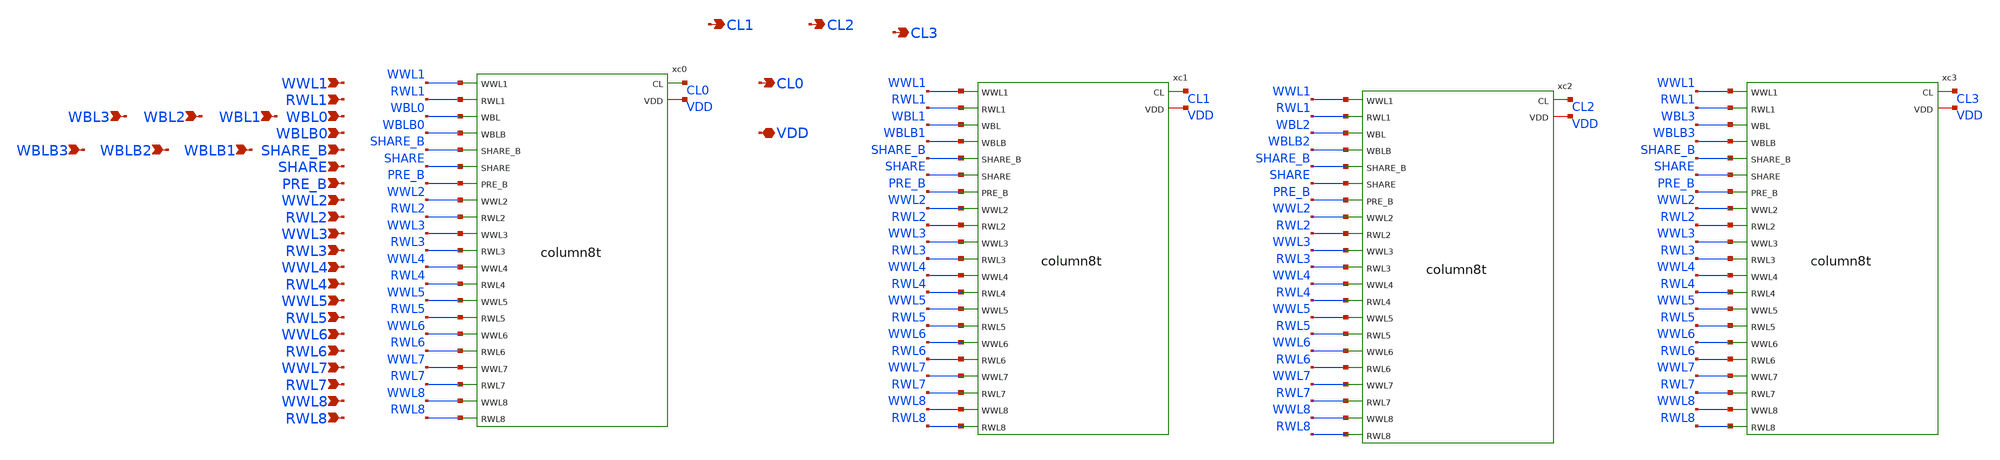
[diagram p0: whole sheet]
** sch_path: schematics/sram_array.sch
**.subckt sram_array WWL1 RWL1 WBL0 WBLB0 SHARE_B SHARE PRE_B WWL2 RWL2 WWL3 RWL3 WWL4 RWL4 WWL5
*+ RWL5 WWL6 RWL6 WWL7 RWL7 WWL8 RWL8 VDD CL0 CL1 CL2 CL3 WBL1 WBL2 WBL3 WBLB1 WBLB2 WBLB3
*.ipin WWL1
*.ipin RWL1
*.ipin WBL0
*.ipin WBLB0
*.ipin SHARE_B
*.ipin SHARE
*.ipin PRE_B
*.ipin WWL2
*.ipin RWL2
*.ipin WWL3
*.ipin RWL3
*.ipin WWL4
*.ipin RWL4
*.ipin WWL5
*.ipin RWL5
*.ipin WWL6
*.ipin RWL6
*.ipin WWL7
*.ipin RWL7
*.ipin WWL8
*.ipin RWL8
*.iopin VDD
*.opin CL0
*.opin CL1
*.opin CL2
*.opin CL3
*.ipin WBL1
*.ipin WBL2
*.ipin WBL3
*.ipin WBLB1
*.ipin WBLB2
*.ipin WBLB3
xc0 CL0 VDD WWL1 RWL1 WBL0 WBLB0 SHARE_B SHARE PRE_B WWL2 RWL2 WWL3 RWL3 WWL4 RWL4 WWL5 RWL5 WWL6
+ RWL6 WWL7 RWL7 WWL8 RWL8 column8t
xc1 CL1 VDD WWL1 RWL1 WBL1 WBLB1 SHARE_B SHARE PRE_B WWL2 RWL2 WWL3 RWL3 WWL4 RWL4 WWL5 RWL5 WWL6
+ RWL6 WWL7 RWL7 WWL8 RWL8 column8t
xc2 CL2 VDD WWL1 RWL1 WBL2 WBLB2 SHARE_B SHARE PRE_B WWL2 RWL2 WWL3 RWL3 WWL4 RWL4 WWL5 RWL5 WWL6
+ RWL6 WWL7 RWL7 WWL8 RWL8 column8t
xc3 CL3 VDD WWL1 RWL1 WBL3 WBLB3 SHARE_B SHARE PRE_B WWL2 RWL2 WWL3 RWL3 WWL4 RWL4 WWL5 RWL5 WWL6
+ RWL6 WWL7 RWL7 WWL8 RWL8 column8t
**.ends
.end
